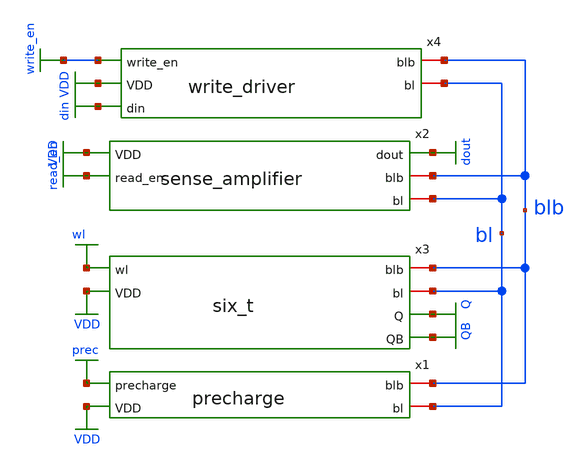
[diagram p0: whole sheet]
** sch_path: xschem/Subcircuits/final_one_bit_sram.sch
**.subckt final_one_bit_sram
x1 prec blb bl VDD precharge
x4 write_en blb bl VDD din write_driver
x3 wl VDD blb bl Q QB six_t
x2 dout VDD blb bl read_en sense_amplifier
**** begin user architecture code


**** begin user architecture code
**change tt at end of .lib line to ss and ff
.lib /home/kaavya/.ciel/ciel/sky130/versions/9233c19260cd813c3fa67dd4594fe4cc67016832/sky130A/libs.tech/ngspice/sky130.lib.spice tt
*------------------------------------------------------------------------------
* SUPPLY, INITIAL STATE, BITLINE LOADS
*------------------------------------------------------------------------------
V1 vdd gnd dc 1.8

.ic v(Q)=1.8 v(QB)=0

Cbl  bl  gnd 100f
Cblb blb gnd 100f

*------------------------------------------------------------------------------
* PRECHARGE (active LOW)
*------------------------------------------------------------------------------
Vprec prec gnd PWL 0n      0 5.00n   0 5.06n   1.8
 20.00n  1.8 20.06n  0 25.00n  0 25.06n  1.8
 40.00n  1.8 40.06n  0 45.00n  0 45.06n  1.8
 60.00n  1.8 60.06n  0 65.00n  0 65.06n  1.8
 80.00n  1.8 80.06n  0 85.00n  0 85.06n  1.8
 95.00n  1.8 95.06n  0 99.00n  0 99.06n  1.8 100n    1.8

*------------------------------------------------------------------------------
* WORDLINE
*------------------------------------------------------------------------------
Vwl wl gnd PWL 0n        0

* Write 0 10.12n    0 10.18n    1.8 16.12n    1.8 16.18n    0

* Read 0 50.12n    0 50.18n    1.8 51.00n    1.8 51.06n    0

* Write 1 70.12n    0 70.18n    1.8 76.12n    1.8 76.18n    0

* Read 1 90.12n    0 90.18n    1.8 91.00n    1.8 91.06n    0
 100n      0

*------------------------------------------------------------------------------
* WRITE ENABLE
*------------------------------------------------------------------------------
Vwrite_en write_en gnd PWL 0n        0

* Write 0 10.26n    0 10.32n    1.8 13.26n    1.8 13.32n    0

* Write 1 70.26n    0 70.32n    1.8 73.26n    1.8 73.32n    0
 100n      0

*------------------------------------------------------------------------------
* READ ENABLE
*------------------------------------------------------------------------------
Vread_en read_en gnd PWL 0n         0

* Read 0 50.26n     0 50.32n     1.8 51.82n     1.8 51.88n     0

* Read 1 90.26n     0 90.32n     1.8 91.82n     1.8 91.88n     0
 100n       0

*------------------------------------------------------------------------------
* DATA IN
*------------------------------------------------------------------------------
Vdin din gnd PWL 0n       0 60.00n   0 60.06n   1.8 100n     1.8

*------------------------------------------------------------------------------
* SIMULATION
*------------------------------------------------------------------------------
.tran 0.1p 100n
.temp 27

*==============================================================================
* 1. WRITE DELAY
*==============================================================================
.meas tran t_write0_50  TRIG v(wl) VAL=0.9 RISE=1 TD=9n  TARG v(Q)  VAL=0.9 FALL=1 TD=9n

.meas tran t_write0_10  TRIG v(wl) VAL=0.9 RISE=1 TD=9n  TARG v(Q)  VAL=0.18 FALL=1 TD=9n

.meas tran t_write1_50  TRIG v(wl) VAL=0.9 RISE=1 TD=69n  TARG v(Q)  VAL=0.9 RISE=1 TD=69n

.meas tran t_write1_90  TRIG v(wl) VAL=0.9 RISE=1 TD=69n  TARG v(Q)  VAL=1.62 RISE=1 TD=69n

*==============================================================================
* 2. FUNCTIONAL CHECKS (read checks just before read_en falls)
*==============================================================================
.meas tran q_after_write0  FIND v(Q)  AT=18n
.meas tran qb_after_write0 FIND v(QB) AT=18n

.meas tran dout_read0 FIND v(dout)   AT=51.6n
.meas tran dg_read0   FIND v(dout_g) AT=51.6n
.meas tran db_read0   FIND v(dout_b) AT=51.6n

.meas tran q_after_write1  FIND v(Q)  AT=78n
.meas tran qb_after_write1 FIND v(QB) AT=78n

.meas tran dout_read1 FIND v(dout)   AT=91.6n
.meas tran dg_read1   FIND v(dout_g) AT=91.6n
.meas tran db_read1   FIND v(dout_b) AT=91.6n

*==============================================================================
* 3. READ TIMING AND OUTPUT CHECKS
*==============================================================================
* read_en -> DOUT (READ 1)
.meas tran t_read1_50  TRIG v(read_en) VAL=0.9 RISE=1 TD=89n  TARG v(dout)    VAL=0.9 RISE=1 TD=89n

.meas tran t_read1_90  TRIG v(read_en) VAL=0.9 RISE=1 TD=89n  TARG v(dout)    VAL=1.62 RISE=1 TD=89n

* Latch resolution (separation of latch nodes reaches 0.8 V)
.meas tran t_res1  TRIG v(read_en) VAL=0.9 RISE=1 TD=89n  TARG par('v(dout_g)-v(dout_b)') VAL=0.8 RISE=1
+ TD=89n

.meas tran t_res0  TRIG v(read_en) VAL=0.9 RISE=1 TD=49n  TARG par('v(dout_b)-v(dout_g)') VAL=0.8 RISE=1
+ TD=49n

* Glitch robustness: DOUT must stay low in READ 0 and high in READ 1
.meas tran dout_max_read0 MAX v(dout) FROM=50.3n TO=51.8n
.meas tran dout_min_read1 MIN v(dout) FROM=91.0n TO=91.8n

*==============================================================================
* 4. READ DISTURB
*==============================================================================
.meas tran q_before_read0 AVG v(Q)  FROM=49n TO=50n
.meas tran q_read0_max MAX v(Q)  FROM=50.18n TO=51.06n
.meas tran read0_disturb  PARAM='q_read0_max-q_before_read0'
* Lowest point of the READ 0 winner node (must stay above the inverter trip point)
.meas tran db_min_read0 MIN v(dout_b) FROM=50.3n TO=51.8n
.meas tran qb_before_read1 AVG v(QB)  FROM=89n TO=90n
.meas tran qb_read1_max MAX v(QB)  FROM=90.18n TO=91.06n
.meas tran read1_disturb  PARAM='qb_read1_max-qb_before_read1'

*==============================================================================
* 5. BITLINE DIFFERENTIAL (sae = at sense enable, wlf = at WL fall)
*==============================================================================
.meas tran bl_sae0  FIND v(bl)  AT=50.32n
.meas tran blb_sae0 FIND v(blb) AT=50.32n
.meas tran dbl_sae0 PARAM='abs(bl_sae0-blb_sae0)'

.meas tran bl_wlf0  FIND v(bl)  AT=51.06n
.meas tran blb_wlf0 FIND v(blb) AT=51.06n
.meas tran dbl_wlf0 PARAM='abs(bl_wlf0-blb_wlf0)'

.meas tran bl_sae1  FIND v(bl)  AT=90.32n
.meas tran blb_sae1 FIND v(blb) AT=90.32n
.meas tran dbl_sae1 PARAM='abs(bl_sae1-blb_sae1)'

.meas tran bl_wlf1  FIND v(bl)  AT=91.06n
.meas tran blb_wlf1 FIND v(blb) AT=91.06n
.meas tran dbl_wlf1 PARAM='abs(bl_wlf1-blb_wlf1)'

*==============================================================================
* 6. ENERGY PER CYCLE (INCLUDING FOLLOWING PRECHARGE)
* i(V1) is negative when the supply delivers current. If energies come out
* negative, remove the minus sign.
*==============================================================================
.meas tran q_w0 INTEG i(V1) FROM=10n TO=30n
.meas tran e_write0 PARAM='-1.8*q_w0'

.meas tran q_r0 INTEG i(V1) FROM=50n TO=68n
.meas tran e_read0 PARAM='-1.8*q_r0'

.meas tran q_w1 INTEG i(V1) FROM=70n TO=88n
.meas tran e_write1 PARAM='-1.8*q_w1'

.meas tran q_r1 INTEG i(V1) FROM=90n TO=100n
.meas tran e_read1 PARAM='-1.8*q_r1'

*==============================================================================
* 7. HOLD CHECK
*==============================================================================
.meas tran q_hold0_avg  AVG v(Q)  FROM=30n TO=39n
.meas tran qb_hold0_avg AVG v(QB) FROM=30n TO=39n
.meas tran q_hold1_avg  AVG v(Q)  FROM=87n TO=89n
.meas tran qb_hold1_avg AVG v(QB) FROM=87n TO=89n

*==============================================================================
* SAVE / CONTROL
*==============================================================================
.save all

.control
run
*remove run - batch mode will not work - run only for plotting the waveforms
plot bl+2 blb
plot prec+8 wl+6
plot write_en+4 read_en+2
plot Q+2 QB
plot dout
*plot dout_g+2 dout_b
.endc
**** end user architecture code



**** end user architecture code
**.ends
.GLOBAL VDD
.GLOBAL wl
.GLOBAL Q
.GLOBAL QB
.GLOBAL prec
.GLOBAL read_en
.GLOBAL dout
.GLOBAL din
.GLOBAL write_en
.end
